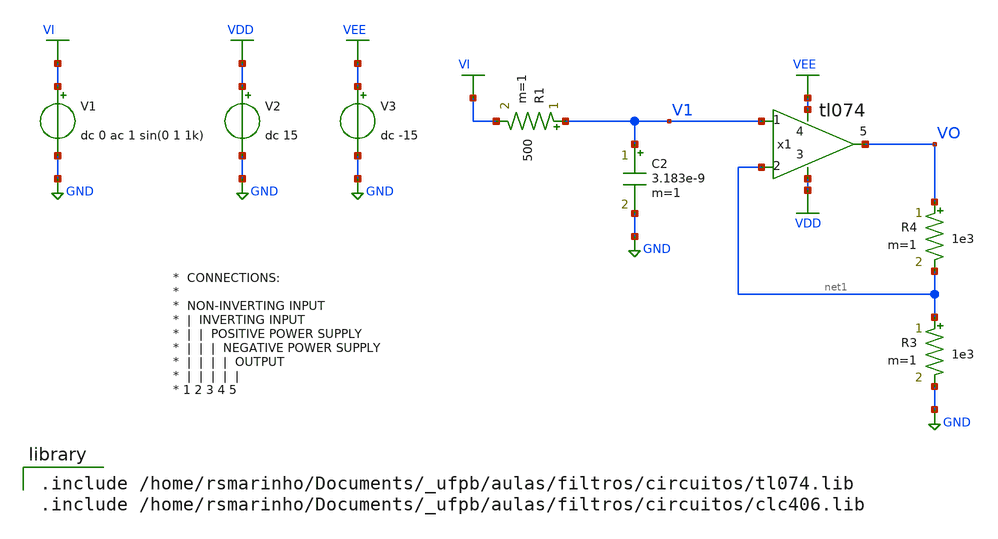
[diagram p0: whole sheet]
** sch_path: circuitos/exemplo10.sch
**.subckt exemplo10
V1 VI GND dc 0 ac 1 sin(0 1 1k)
R4 VO net1 1e3 m=1
R3 net1 GND 1e3 m=1
V2 VDD GND dc 15
V3 VEE GND dc -15
R1 V1 VI 500 m=1
C2 V1 GND 3.183e-9 m=1
x1 V1 net1 VDD VEE VO tl074
**** begin user architecture code

.include /home/rsmarinho/Documents/_ufpb/aulas/filtros/circuitos/tl074.lib
.include /home/rsmarinho/Documents/_ufpb/aulas/filtros/circuitos/clc406.lib


.control

ac dec 1e2 1e2 1e9
plot xlog db(v(vo)/v(vi))

tran 1e-6 2e-3
plot vi vo

alter @v1[sin] [ 0 1 170k ]
tran 1e-6 2e-3
plot vi vo

alter r3 1e12
alter r4 1e-6
ac dec 1e2 1e2 1e9
plot xlog db(v(vo)/v(vi))

.endc
.end

**** end user architecture code
**.ends
.GLOBAL GND
.GLOBAL VDD
.GLOBAL VI
.GLOBAL VEE
.end
